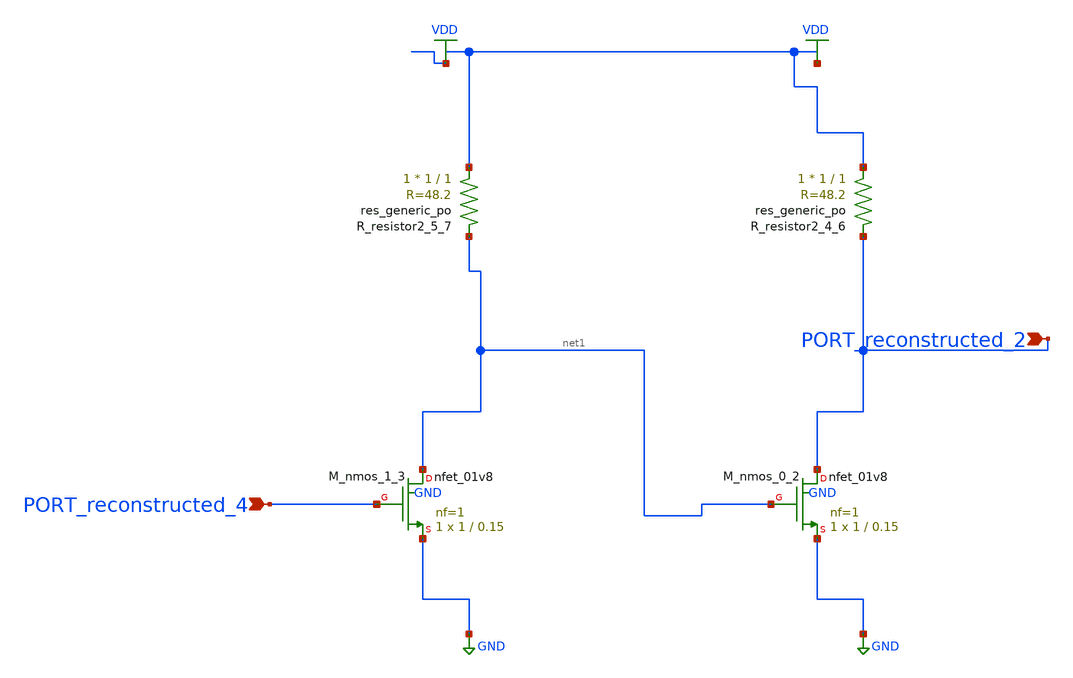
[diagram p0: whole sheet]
** sch_path: schematics/AMSNet/303.sch
**.subckt 303 PORT_reconstructed_2 PORT_reconstructed_4
*.ipin PORT_reconstructed_2
*.ipin PORT_reconstructed_4
XM_nmos_0_2 PORT_reconstructed_2 net1 GND GND sky130_fd_pr__nfet_01v8 L=0.15 W=1 nf=1 ad='int((1 + 1)/2) * 1 / 1 * 0.29'
+ as='int((1 + 2)/2) * 1 / 1 * 0.29' pd='2*int((1 + 1)/2) * (1 / 1 + 0.29)' ps='2*int((1 + 2)/2) * (1 / 1 + 0.29)'
+ nrd='0.29 / 1 ' nrs='0.29 / 1 ' sa=0 sb=0 sd=0 mult=1 m=1
XM_nmos_1_3 net1 PORT_reconstructed_4 GND GND sky130_fd_pr__nfet_01v8 L=0.15 W=1 nf=1 ad='int((1 + 1)/2) * 1 / 1 * 0.29'
+ as='int((1 + 2)/2) * 1 / 1 * 0.29' pd='2*int((1 + 1)/2) * (1 / 1 + 0.29)' ps='2*int((1 + 2)/2) * (1 / 1 + 0.29)'
+ nrd='0.29 / 1 ' nrs='0.29 / 1 ' sa=0 sb=0 sd=0 mult=1 m=1
XR_resistor2_4_6 VDD PORT_reconstructed_2 sky130_fd_pr__res_generic_po W=1 L=1 m=1
XR_resistor2_5_7 VDD net1 sky130_fd_pr__res_generic_po W=1 L=1 m=1
**.ends
.GLOBAL GND
.GLOBAL VDD
.end
